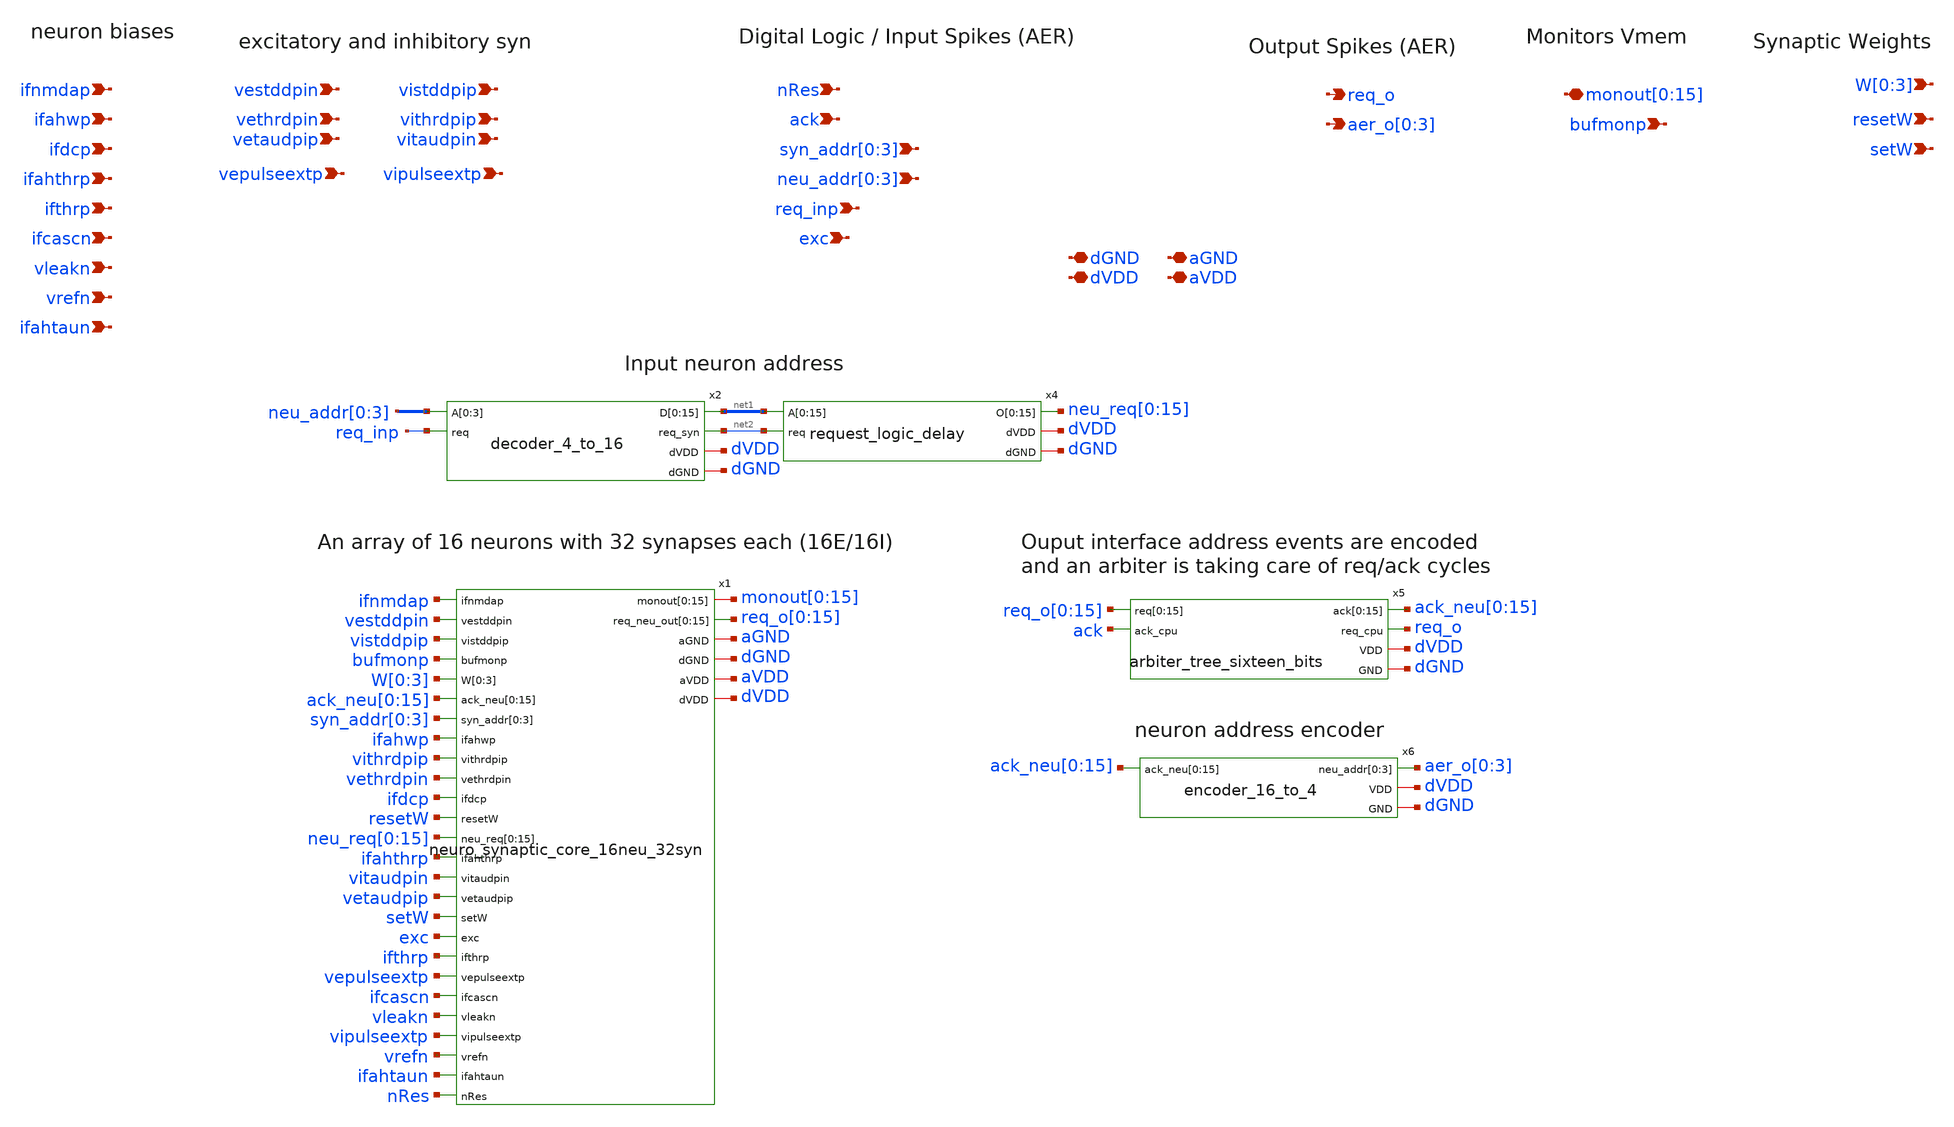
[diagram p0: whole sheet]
** sch_path: design/xschem/neuron_synapse_array_with_input_output_logic.sch
**.subckt neuron_synapse_array_with_input_output_logic vleakn vrefn ifahtaun ifcascn ifthrp ifahthrp
*+ ifdcp ifahwp ifnmdap vestddpin vethrdpin vetaudpip vistddpip vithrdpip vitaudpin vepulseextp bufmonp
*+ vipulseextp req_o aer_o[0],aer_o[1],aer_o[2],aer_o[3] dGND dVDD nRes ack
*+ neu_addr[0],neu_addr[1],neu_addr[2],neu_addr[3] req_inp syn_addr[0],syn_addr[1],syn_addr[2],syn_addr[3] exc aGND aVDD
*+ monout[0],monout[1],monout[2],monout[3],monout[4],monout[5],monout[6],monout[7],monout[8],monout[9],monout[10],monout[11],monout[12],monout[13],monout[14],monout[15] W[0],W[1],W[2],W[3] resetW setW
*.ipin vleakn
*.ipin vrefn
*.ipin ifahtaun
*.ipin ifcascn
*.ipin ifthrp
*.ipin ifahthrp
*.ipin ifdcp
*.ipin ifahwp
*.ipin ifnmdap
*.ipin vestddpin
*.ipin vethrdpin
*.ipin vetaudpip
*.ipin vistddpip
*.ipin vithrdpip
*.ipin vitaudpin
*.ipin vepulseextp
*.ipin bufmonp
*.ipin vipulseextp
*.opin req_o
*.opin aer_o[0],aer_o[1],aer_o[2],aer_o[3]
*.iopin dGND
*.iopin dVDD
*.ipin nRes
*.ipin ack
*.ipin neu_addr[0],neu_addr[1],neu_addr[2],neu_addr[3]
*.ipin req_inp
*.ipin syn_addr[0],syn_addr[1],syn_addr[2],syn_addr[3]
*.ipin exc
*.iopin aGND
*.iopin aVDD
*.iopin
*+ monout[0],monout[1],monout[2],monout[3],monout[4],monout[5],monout[6],monout[7],monout[8],monout[9],monout[10],monout[11],monout[12],monout[13],monout[14],monout[15]
*.ipin W[0],W[1],W[2],W[3]
*.ipin resetW
*.ipin setW
x1 ifnmdap vestddpin vistddpip bufmonp W[0] W[1] W[2] W[3] ack_neu[0] ack_neu[1] ack_neu[2]
+ ack_neu[3] ack_neu[4] ack_neu[5] ack_neu[6] ack_neu[7] ack_neu[8] ack_neu[9] ack_neu[10] ack_neu[11]
+ ack_neu[12] ack_neu[13] ack_neu[14] ack_neu[15] syn_addr[0] syn_addr[1] syn_addr[2] syn_addr[3] ifahwp
+ monout[0] monout[1] monout[2] monout[3] monout[4] monout[5] monout[6] monout[7] monout[8] monout[9]
+ monout[10] monout[11] monout[12] monout[13] monout[14] monout[15] vithrdpip vethrdpin ifdcp resetW neu_req[0]
+ neu_req[1] neu_req[2] neu_req[3] neu_req[4] neu_req[5] neu_req[6] neu_req[7] neu_req[8] neu_req[9] neu_req[10]
+ neu_req[11] neu_req[12] neu_req[13] neu_req[14] neu_req[15] ifahthrp req_o[0] req_o[1] req_o[2] req_o[3]
+ req_o[4] req_o[5] req_o[6] req_o[7] req_o[8] req_o[9] req_o[10] req_o[11] req_o[12] req_o[13] req_o[14]
+ req_o[15] vitaudpin vetaudpip setW exc ifthrp vepulseextp ifcascn vleakn vipulseextp aGND dGND vrefn aVDD
+ dVDD ifahtaun nRes neuro_synaptic_core_16neu_32syn
x2 neu_addr[0] neu_addr[1] neu_addr[2] neu_addr[3] net1[15] net1[14] net1[13] net1[12] net1[11]
+ net1[10] net1[9] net1[8] net1[7] net1[6] net1[5] net1[4] net1[3] net1[2] net1[1] net1[0] req_inp net2 dVDD
+ dGND decoder_4_to_16
x4 net1[15] net1[14] net1[13] net1[12] net1[11] net1[10] net1[9] net1[8] net1[7] net1[6] net1[5]
+ net1[4] net1[3] net1[2] net1[1] net1[0] neu_req[0] neu_req[1] neu_req[2] neu_req[3] neu_req[4] neu_req[5]
+ neu_req[6] neu_req[7] neu_req[8] neu_req[9] neu_req[10] neu_req[11] neu_req[12] neu_req[13] neu_req[14]
+ neu_req[15] net2 dVDD dGND request_logic_delay
x5 req_o[0] req_o[1] req_o[2] req_o[3] req_o[4] req_o[5] req_o[6] req_o[7] req_o[8] req_o[9]
+ req_o[10] req_o[11] req_o[12] req_o[13] req_o[14] req_o[15] ack ack_neu[0] ack_neu[1] ack_neu[2] ack_neu[3]
+ ack_neu[4] ack_neu[5] ack_neu[6] ack_neu[7] ack_neu[8] ack_neu[9] ack_neu[10] ack_neu[11] ack_neu[12]
+ ack_neu[13] ack_neu[14] ack_neu[15] req_o dVDD dGND arbiter_tree_sixteen_bits
x6 aer_o[0] aer_o[1] aer_o[2] aer_o[3] ack_neu[0] ack_neu[1] ack_neu[2] ack_neu[3] ack_neu[4]
+ ack_neu[5] ack_neu[6] ack_neu[7] ack_neu[8] ack_neu[9] ack_neu[10] ack_neu[11] ack_neu[12] ack_neu[13]
+ ack_neu[14] ack_neu[15] dVDD dGND encoder_16_to_4
**.ends
.end
